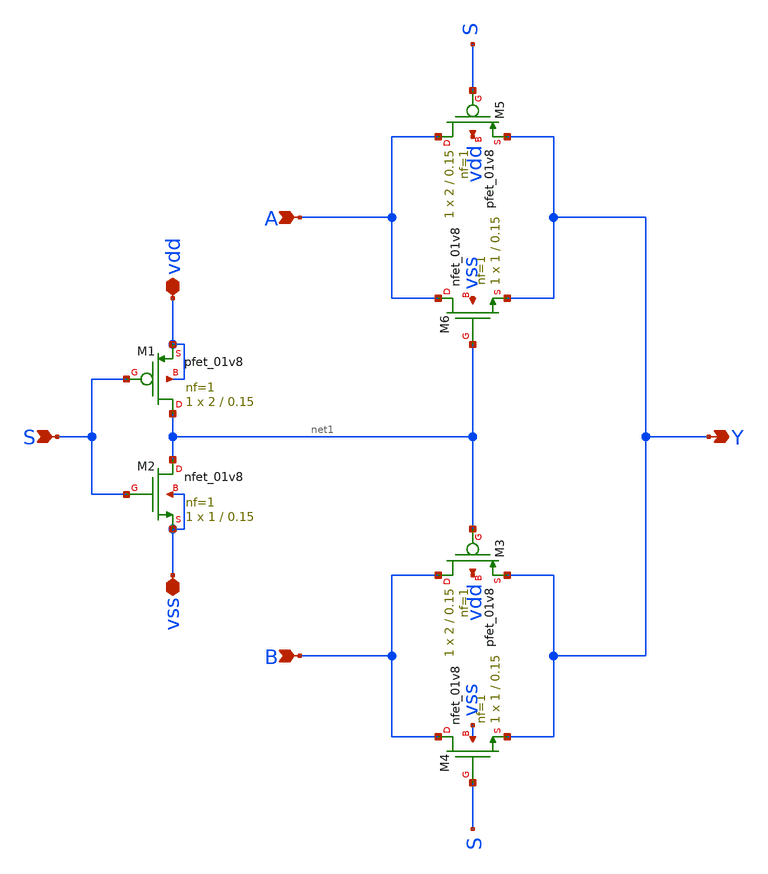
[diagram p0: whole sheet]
** sch_path: xsch/ip/tmux/tmux_2to1.sch
**.subckt tmux_2to1 Y S vss vdd A B
*.opin Y
*.ipin S
*.iopin vss
*.iopin vdd
*.ipin A
*.ipin B
XM1 net1 S vdd vdd sky130_fd_pr__pfet_01v8 L=0.15 W=2 nf=1 ad='int((1 + 1)/2) * 2 / 1 * 0.29' as='int((1 + 2)/2) * 2 / 1 * 0.29'
+ pd='2*int((1 + 1)/2) * (2 / 1 + 0.29)' ps='2*int((1 + 2)/2) * (2 / 1 + 0.29)' nrd='0.29 / 2 ' nrs='0.29 / 2 '
+ sa=0 sb=0 sd=0 mult=1 m=1
XM2 net1 S vss vss sky130_fd_pr__nfet_01v8 L=0.15 W=1 nf=1 ad='int((1 + 1)/2) * 1 / 1 * 0.29' as='int((1 + 2)/2) * 1 / 1 * 0.29'
+ pd='2*int((1 + 1)/2) * (1 / 1 + 0.29)' ps='2*int((1 + 2)/2) * (1 / 1 + 0.29)' nrd='0.29 / 1 ' nrs='0.29 / 1 '
+ sa=0 sb=0 sd=0 mult=1 m=1
XM3 B net1 Y vdd sky130_fd_pr__pfet_01v8 L=0.15 W=2 nf=1 ad='int((1 + 1)/2) * 2 / 1 * 0.29' as='int((1 + 2)/2) * 2 / 1 * 0.29'
+ pd='2*int((1 + 1)/2) * (2 / 1 + 0.29)' ps='2*int((1 + 2)/2) * (2 / 1 + 0.29)' nrd='0.29 / 2 ' nrs='0.29 / 2 '
+ sa=0 sb=0 sd=0 mult=1 m=1
XM4 B S Y vss sky130_fd_pr__nfet_01v8 L=0.15 W=1 nf=1 ad='int((1 + 1)/2) * 1 / 1 * 0.29' as='int((1 + 2)/2) * 1 / 1 * 0.29'
+ pd='2*int((1 + 1)/2) * (1 / 1 + 0.29)' ps='2*int((1 + 2)/2) * (1 / 1 + 0.29)' nrd='0.29 / 1 ' nrs='0.29 / 1 '
+ sa=0 sb=0 sd=0 mult=1 m=1
XM5 A S Y vdd sky130_fd_pr__pfet_01v8 L=0.15 W=2 nf=1 ad='int((1 + 1)/2) * 2 / 1 * 0.29' as='int((1 + 2)/2) * 2 / 1 * 0.29'
+ pd='2*int((1 + 1)/2) * (2 / 1 + 0.29)' ps='2*int((1 + 2)/2) * (2 / 1 + 0.29)' nrd='0.29 / 2 ' nrs='0.29 / 2 '
+ sa=0 sb=0 sd=0 mult=1 m=1
XM6 A net1 Y vss sky130_fd_pr__nfet_01v8 L=0.15 W=1 nf=1 ad='int((1 + 1)/2) * 1 / 1 * 0.29' as='int((1 + 2)/2) * 1 / 1 * 0.29'
+ pd='2*int((1 + 1)/2) * (1 / 1 + 0.29)' ps='2*int((1 + 2)/2) * (1 / 1 + 0.29)' nrd='0.29 / 1 ' nrs='0.29 / 1 '
+ sa=0 sb=0 sd=0 mult=1 m=1
**.ends
.end
